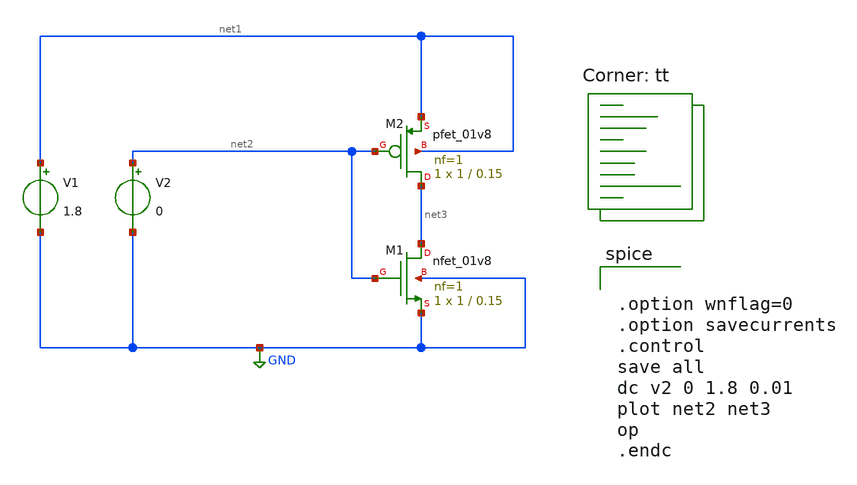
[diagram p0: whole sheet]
** sch_path: inv_tb.sch
**.subckt inv_tb
XM1 net3 net2 GND GND sky130_fd_pr__nfet_01v8 L=0.15 W=1 nf=1 ad='int((nf+1)/2) * W/nf * 0.29' as='int((nf+2)/2) * W/nf * 0.29'
+ pd='2*int((nf+1)/2) * (W/nf + 0.29)' ps='2*int((nf+2)/2) * (W/nf + 0.29)' nrd='0.29 / W' nrs='0.29 / W'
+ sa=0 sb=0 sd=0 mult=1 m=1
XM2 net3 net2 net1 net1 sky130_fd_pr__pfet_01v8 L=0.15 W=1 nf=1 ad='int((nf+1)/2) * W/nf * 0.29' as='int((nf+2)/2) * W/nf * 0.29'
+ pd='2*int((nf+1)/2) * (W/nf + 0.29)' ps='2*int((nf+2)/2) * (W/nf + 0.29)' nrd='0.29 / W' nrs='0.29 / W'
+ sa=0 sb=0 sd=0 mult=1 m=1
V1 net1 GND 1.8
V2 net2 GND 0
**** begin user architecture code
.lib $::SKYWATER_MODELS/sky130.lib.spice tt


.option wnflag=0
.option savecurrents
.control
save all
dc v2 0 1.8 0.01
plot net2 net3
op
.endc


**** end user architecture code
**.ends
.GLOBAL GND
.end
